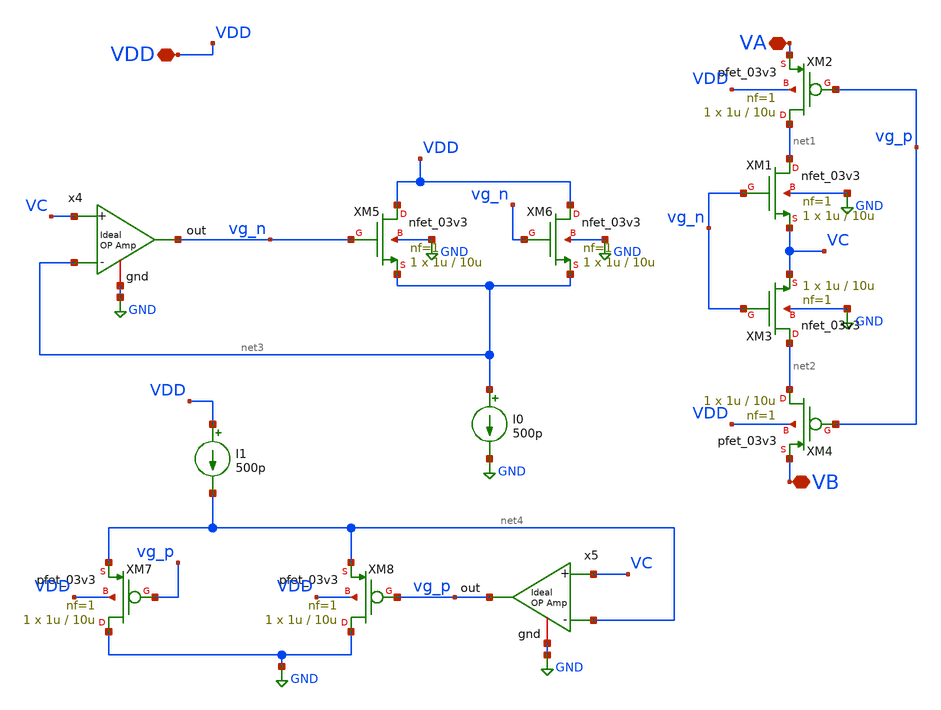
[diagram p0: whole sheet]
** sch_path: TIA/xschem/pseudo_res_dir/PR_PMOS_NMOS.sch
**.subckt PR_PMOS_NMOS VA VB VDD
*.iopin VA
*.iopin VB
*.iopin VDD
XM1 net1 vg_n VC GND nfet_03v3 L=10u W=1u nf=1 ad='int((nf+1)/2) * W/nf * 0.18u' as='int((nf+2)/2) * W/nf * 0.18u'
+ pd='2*int((nf+1)/2) * (W/nf + 0.18u)' ps='2*int((nf+2)/2) * (W/nf + 0.18u)' nrd='0.18u / W' nrs='0.18u / W'
+ sa=0 sb=0 sd=0 m=1
XM2 net1 vg_p VA VDD pfet_03v3 L=10u W=1u nf=1 ad='int((nf+1)/2) * W/nf * 0.18u' as='int((nf+2)/2) * W/nf * 0.18u'
+ pd='2*int((nf+1)/2) * (W/nf + 0.18u)' ps='2*int((nf+2)/2) * (W/nf + 0.18u)' nrd='0.18u / W' nrs='0.18u / W'
+ sa=0 sb=0 sd=0 m=1
XM3 net2 vg_n VC GND nfet_03v3 L=10u W=1u nf=1 ad='int((nf+1)/2) * W/nf * 0.18u' as='int((nf+2)/2) * W/nf * 0.18u'
+ pd='2*int((nf+1)/2) * (W/nf + 0.18u)' ps='2*int((nf+2)/2) * (W/nf + 0.18u)' nrd='0.18u / W' nrs='0.18u / W'
+ sa=0 sb=0 sd=0 m=1
XM4 net2 vg_p VB VDD pfet_03v3 L=10u W=1u nf=1 ad='int((nf+1)/2) * W/nf * 0.18u' as='int((nf+2)/2) * W/nf * 0.18u'
+ pd='2*int((nf+1)/2) * (W/nf + 0.18u)' ps='2*int((nf+2)/2) * (W/nf + 0.18u)' nrd='0.18u / W' nrs='0.18u / W'
+ sa=0 sb=0 sd=0 m=1
XM5 VDD vg_n net3 GND nfet_03v3 L=10u W=1u nf=1 ad='int((nf+1)/2) * W/nf * 0.18u' as='int((nf+2)/2) * W/nf * 0.18u'
+ pd='2*int((nf+1)/2) * (W/nf + 0.18u)' ps='2*int((nf+2)/2) * (W/nf + 0.18u)' nrd='0.18u / W' nrs='0.18u / W'
+ sa=0 sb=0 sd=0 m=1
XM6 VDD vg_n net3 GND nfet_03v3 L=10u W=1u nf=1 ad='int((nf+1)/2) * W/nf * 0.18u' as='int((nf+2)/2) * W/nf * 0.18u'
+ pd='2*int((nf+1)/2) * (W/nf + 0.18u)' ps='2*int((nf+2)/2) * (W/nf + 0.18u)' nrd='0.18u / W' nrs='0.18u / W'
+ sa=0 sb=0 sd=0 m=1
XM7 GND vg_p net4 VDD pfet_03v3 L=10u W=1u nf=1 ad='int((nf+1)/2) * W/nf * 0.18u' as='int((nf+2)/2) * W/nf * 0.18u'
+ pd='2*int((nf+1)/2) * (W/nf + 0.18u)' ps='2*int((nf+2)/2) * (W/nf + 0.18u)' nrd='0.18u / W' nrs='0.18u / W'
+ sa=0 sb=0 sd=0 m=1
XM8 GND vg_p net4 VDD pfet_03v3 L=10u W=1u nf=1 ad='int((nf+1)/2) * W/nf * 0.18u' as='int((nf+2)/2) * W/nf * 0.18u'
+ pd='2*int((nf+1)/2) * (W/nf + 0.18u)' ps='2*int((nf+2)/2) * (W/nf + 0.18u)' nrd='0.18u / W' nrs='0.18u / W'
+ sa=0 sb=0 sd=0 m=1
I0 net3 GND 500p
I1 VDD net4 500p
x4 vg_n VC net3 GND ampOp_ideal
x5 vg_p VC net4 GND ampOp_ideal
**.ends

* expanding   symbol:  /home/gmaranhao/Desktop/gf180_work/auxLib/ampOp_ideal.sym # of pins=4
** sym_path: /home/gmaranhao/Desktop/gf180_work/auxLib/ampOp_ideal.sym
** sch_path: /home/gmaranhao/Desktop/gf180_work/auxLib/ampOp_ideal.sch
.subckt ampOp_ideal out + - gnd
*.ipin +
*.ipin -
*.opin out
*.iopin gnd
E1 out gnd + - 10000000
.ends

.GLOBAL GND
.end
